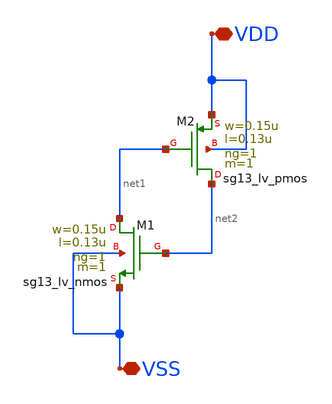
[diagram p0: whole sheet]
** sch_path: ADC8711-main/schematic/xschem/Decap_Cell.sch
**.subckt Decap_Cell VDD VSS
*.iopin VDD
*.iopin VSS
XM1 net1 net2 VSS VSS sg13_lv_nmos w=0.15u l=0.13u ng=1 m=1 mm_ok=1
XM2 net2 net1 VDD VDD sg13_lv_pmos w=0.15u l=0.13u ng=1 m=1 mm_ok=1
**.ends
.end
